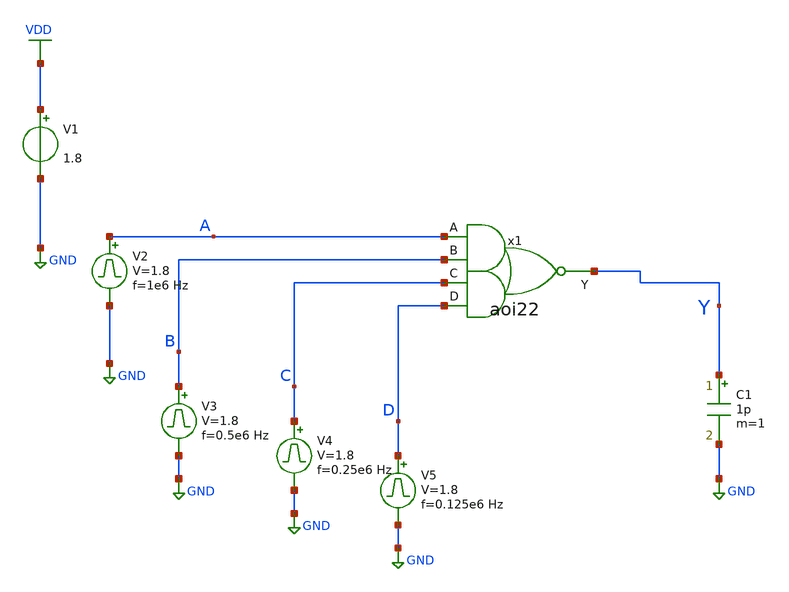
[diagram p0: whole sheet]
** sch_path: xschem/aoi22_tb.sch
**.subckt aoi22_tb
V1 VDD GND 1.8
V2 A GND pulse 0 1.8 '0.495/ 1e6 ' '0.01/1e6 ' '0.01/1e6 ' '0.49/1e6 ' '1/1e6 '
C1 Y GND 1p m=1
V3 B GND pulse 0 1.8 '0.495/ 0.5e6 ' '0.01/0.5e6 ' '0.01/0.5e6 ' '0.49/0.5e6 ' '1/0.5e6 '
x1 C D A B Y aoi22
V4 C GND pulse 0 1.8 '0.495/ 0.25e6 ' '0.01/0.25e6 ' '0.01/0.25e6 ' '0.49/0.25e6 ' '1/0.25e6 '
V5 D GND pulse 0 1.8 '0.495/ 0.125e6 ' '0.01/0.125e6 ' '0.01/0.125e6 ' '0.49/0.125e6 ' '1/0.125e6 '
**** begin user architecture code


.control
save all
tran 1n 8u
plot V(A) V(B)+2 V(C)+4 V(D)+6 V(Y)+8
.endc



** opencircuitdesign pdks install
.lib $::SKYWATER_MODELS/sky130.lib.spice tt


**** end user architecture code
**.ends

* expanding   symbol:  aoi22.sym # of pins=5
** sym_path: xschem/aoi22.sym
** sch_path: xschem/aoi22.sch
.subckt aoi22 C D A B Y
*.opin Y
*.ipin C
*.ipin A
*.ipin D
*.ipin B
XM1 Y B net1 GND sky130_fd_pr__nfet_01v8 L=0.15 W=0.5 nf=1 ad='int((nf+1)/2) * W/nf * 0.29' as='int((nf+2)/2) * W/nf * 0.29'
+ pd='2*int((nf+1)/2) * (W/nf + 0.29)' ps='2*int((nf+2)/2) * (W/nf + 0.29)' nrd='0.29 / W' nrs='0.29 / W'
+ sa=0 sb=0 sd=0 mult=1 m=1
XM2 net2 D VDD VDD sky130_fd_pr__pfet_01v8 L=0.15 W=1 nf=1 ad='int((nf+1)/2) * W/nf * 0.29' as='int((nf+2)/2) * W/nf * 0.29'
+ pd='2*int((nf+1)/2) * (W/nf + 0.29)' ps='2*int((nf+2)/2) * (W/nf + 0.29)' nrd='0.29 / W' nrs='0.29 / W'
+ sa=0 sb=0 sd=0 mult=1 m=1
XM3 net2 C VDD VDD sky130_fd_pr__pfet_01v8 L=0.15 W=1 nf=1 ad='int((nf+1)/2) * W/nf * 0.29' as='int((nf+2)/2) * W/nf * 0.29'
+ pd='2*int((nf+1)/2) * (W/nf + 0.29)' ps='2*int((nf+2)/2) * (W/nf + 0.29)' nrd='0.29 / W' nrs='0.29 / W'
+ sa=0 sb=0 sd=0 mult=1 m=1
XM4 Y D net1 GND sky130_fd_pr__nfet_01v8 L=0.15 W=0.5 nf=1 ad='int((nf+1)/2) * W/nf * 0.29' as='int((nf+2)/2) * W/nf * 0.29'
+ pd='2*int((nf+1)/2) * (W/nf + 0.29)' ps='2*int((nf+2)/2) * (W/nf + 0.29)' nrd='0.29 / W' nrs='0.29 / W'
+ sa=0 sb=0 sd=0 mult=1 m=1
XM5 net1 A GND GND sky130_fd_pr__nfet_01v8 L=0.15 W=0.5 nf=1 ad='int((nf+1)/2) * W/nf * 0.29' as='int((nf+2)/2) * W/nf * 0.29'
+ pd='2*int((nf+1)/2) * (W/nf + 0.29)' ps='2*int((nf+2)/2) * (W/nf + 0.29)' nrd='0.29 / W' nrs='0.29 / W'
+ sa=0 sb=0 sd=0 mult=1 m=1
XM6 net1 C GND GND sky130_fd_pr__nfet_01v8 L=0.15 W=0.5 nf=1 ad='int((nf+1)/2) * W/nf * 0.29' as='int((nf+2)/2) * W/nf * 0.29'
+ pd='2*int((nf+1)/2) * (W/nf + 0.29)' ps='2*int((nf+2)/2) * (W/nf + 0.29)' nrd='0.29 / W' nrs='0.29 / W'
+ sa=0 sb=0 sd=0 mult=1 m=1
XM7 Y B net2 VDD sky130_fd_pr__pfet_01v8 L=0.15 W=1 nf=1 ad='int((nf+1)/2) * W/nf * 0.29' as='int((nf+2)/2) * W/nf * 0.29'
+ pd='2*int((nf+1)/2) * (W/nf + 0.29)' ps='2*int((nf+2)/2) * (W/nf + 0.29)' nrd='0.29 / W' nrs='0.29 / W'
+ sa=0 sb=0 sd=0 mult=1 m=1
XM8 Y A net2 VDD sky130_fd_pr__pfet_01v8 L=0.15 W=1 nf=1 ad='int((nf+1)/2) * W/nf * 0.29' as='int((nf+2)/2) * W/nf * 0.29'
+ pd='2*int((nf+1)/2) * (W/nf + 0.29)' ps='2*int((nf+2)/2) * (W/nf + 0.29)' nrd='0.29 / W' nrs='0.29 / W'
+ sa=0 sb=0 sd=0 mult=1 m=1
.ends

.GLOBAL VDD
.GLOBAL GND
.end
